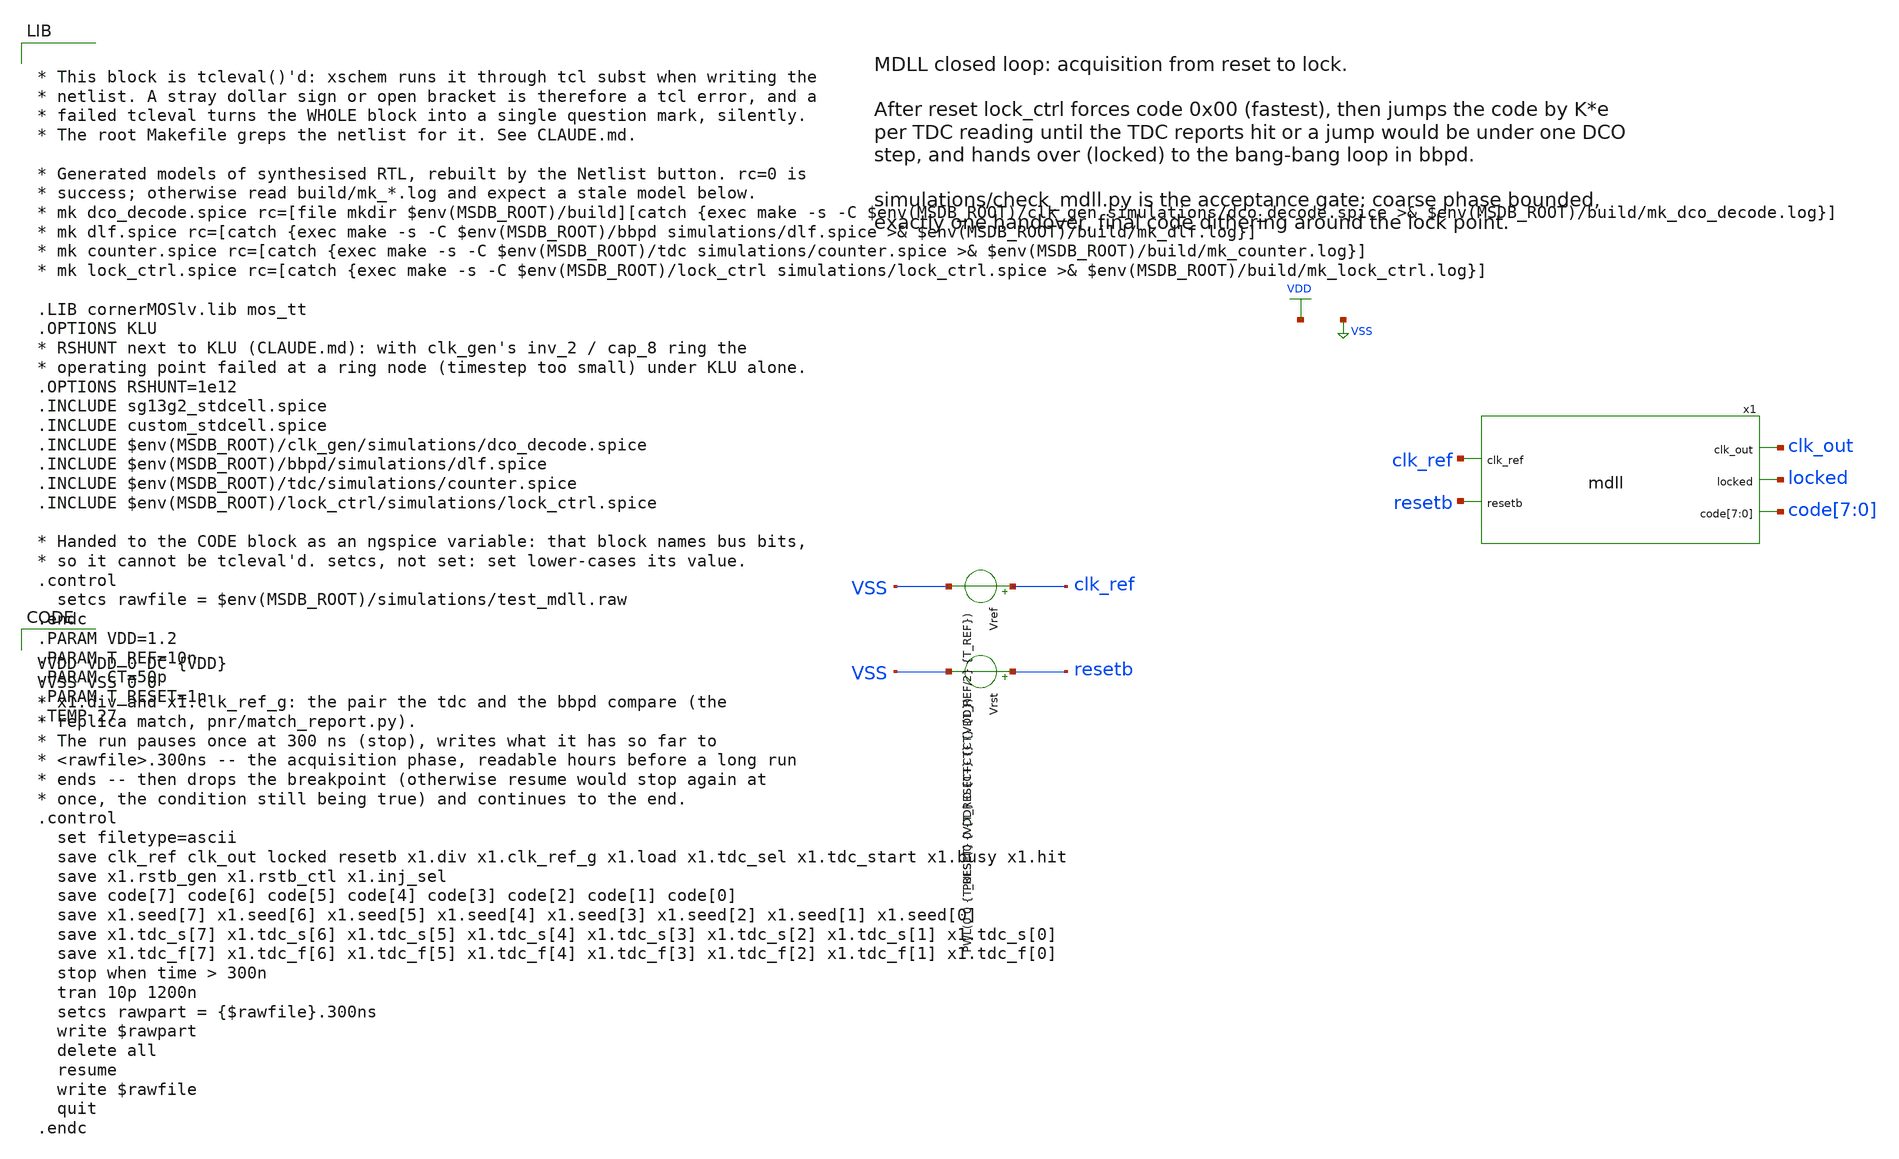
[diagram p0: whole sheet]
** sch_path: TPU5555-main/mdll/mixed_signal_design_blocks/test_mdll.sch


* This block is tcleval()'d: xschem runs it through tcl subst when writing the
* netlist. A stray dollar sign or open bracket is therefore a tcl error, and a
* failed tcleval turns the WHOLE block into a single question mark, silently.
* The root Makefile greps the netlist for it. See CLAUDE.md.

* Generated models of synthesised RTL, rebuilt by the Netlist button. rc=0 is
* success; otherwise read build/mk_*.log and expect a stale model below.
* mk dco_decode.spice rc=[file mkdir $env(MSDB_ROOT)/build][catch {exec make -s -C $env(MSDB_ROOT)/clk_gen
*+ simulations/dco_decode.spice >& $env(MSDB_ROOT)/build/mk_dco_decode.log}]
* mk dlf.spice rc=[catch {exec make -s -C $env(MSDB_ROOT)/bbpd simulations/dlf.spice >& $env(MSDB_ROOT)/build/mk_dlf.log}]
* mk counter.spice rc=[catch {exec make -s -C $env(MSDB_ROOT)/tdc simulations/counter.spice >& $env(MSDB_ROOT)/build/mk_counter.log}]
* mk lock_ctrl.spice rc=[catch {exec make -s -C $env(MSDB_ROOT)/lock_ctrl simulations/lock_ctrl.spice
*+ >& $env(MSDB_ROOT)/build/mk_lock_ctrl.log}]

.LIB cornerMOSlv.lib mos_tt
.OPTIONS KLU
* RSHUNT next to KLU (CLAUDE.md): with clk_gen's inv_2 / cap_8 ring the
* operating point failed at a ring node (timestep too small) under KLU alone.
.OPTIONS RSHUNT=1e12
.INCLUDE sg13g2_stdcell.spice
.INCLUDE custom_stdcell.spice
.INCLUDE $env(MSDB_ROOT)/clk_gen/simulations/dco_decode.spice
.INCLUDE $env(MSDB_ROOT)/bbpd/simulations/dlf.spice
.INCLUDE $env(MSDB_ROOT)/tdc/simulations/counter.spice
.INCLUDE $env(MSDB_ROOT)/lock_ctrl/simulations/lock_ctrl.spice

* Handed to the CODE block as an ngspice variable: that block names bus bits,
* so it cannot be tcleval'd. setcs, not set: set lower-cases its value.
.control
  setcs rawfile = $env(MSDB_ROOT)/simulations/test_mdll.raw
.endc
.PARAM VDD=1.2
.PARAM T_REF=10n
.PARAM CT=50p
.PARAM T_RESET=1n
.TEMP 27


**.subckt test_mdll
x1 clk_ref resetb clk_out locked code[7] code[6] code[5] code[4] code[3] code[2] code[1] code[0] mdll
Vref clk_ref VSS PULSE(0 {VDD} 0 {CT} {CT} {T_REF/2} {T_REF})
Vrst resetb VSS PWL(0 0 {T_RESET} 0 {T_RESET+CT} {VDD})
**** begin user architecture code


VVDD VDD 0 DC {VDD}
VVSS VSS 0 0
* x1.div and x1.clk_ref_g: the pair the tdc and the bbpd compare (the
* replica match, pnr/match_report.py).
* The run pauses once at 300 ns (stop), writes what it has so far to
* <rawfile>.300ns -- the acquisition phase, readable hours before a long run
* ends -- then drops the breakpoint (otherwise resume would stop again at
* once, the condition still being true) and continues to the end.
.control
  set filetype=ascii
  save clk_ref clk_out locked resetb x1.div x1.clk_ref_g x1.load x1.tdc_sel x1.tdc_start x1.busy x1.hit
  save x1.rstb_gen x1.rstb_ctl x1.inj_sel
  save code[7] code[6] code[5] code[4] code[3] code[2] code[1] code[0]
  save x1.seed[7] x1.seed[6] x1.seed[5] x1.seed[4] x1.seed[3] x1.seed[2] x1.seed[1] x1.seed[0]
  save x1.tdc_s[7] x1.tdc_s[6] x1.tdc_s[5] x1.tdc_s[4] x1.tdc_s[3] x1.tdc_s[2] x1.tdc_s[1] x1.tdc_s[0]
  save x1.tdc_f[7] x1.tdc_f[6] x1.tdc_f[5] x1.tdc_f[4] x1.tdc_f[3] x1.tdc_f[2] x1.tdc_f[1] x1.tdc_f[0]
  stop when time > 300n
  tran 10p 1200n
  setcs rawpart = {$rawfile}.300ns
  write $rawpart
  delete all
  resume
  write $rawfile
  quit
.endc


**** end user architecture code
**.ends
.GLOBAL VDD
.GLOBAL VSS
.end
